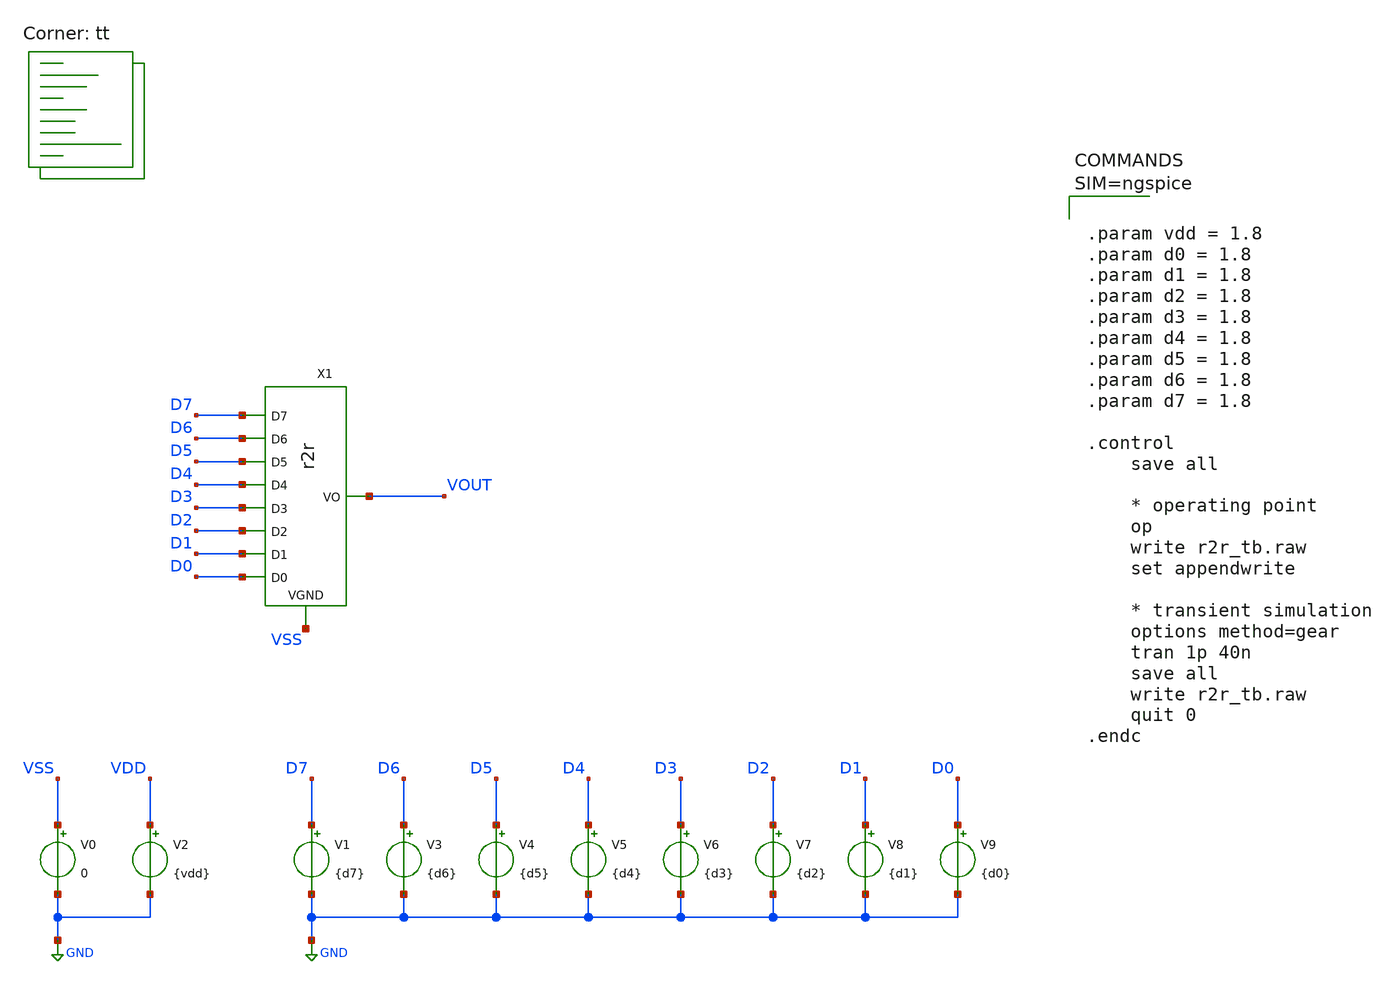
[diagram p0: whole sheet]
** sch_path: xschem/r2r_tb.sch
**.subckt r2r_tb
X1 D7 D6 D5 D4 D3 D2 D1 D0 VOUT VSS r2r
V0 VSS GND 0
V2 VDD GND {vdd}
V3 D6 GND {d6}
V1 D7 GND {d7}
V4 D5 GND {d5}
V5 D4 GND {d4}
V6 D3 GND {d3}
V7 D2 GND {d2}
V8 D1 GND {d1}
V9 D0 GND {d0}
**** begin user architecture code



.param vdd = 1.8
.param d0 = 1.8
.param d1 = 1.8
.param d2 = 1.8
.param d3 = 1.8
.param d4 = 1.8
.param d5 = 1.8
.param d6 = 1.8
.param d7 = 1.8

.control
    save all

    * operating point
    op
    write r2r_tb.raw
    set appendwrite

    * transient simulation
    options method=gear
    tran 1p 40n
    save all
    write r2r_tb.raw
    quit 0
.endc



.lib $::SKYWATER_MODELS/sky130.lib.spice tt
**** end user architecture code
**.ends

* expanding   symbol:  /home/unixpoly/analog/projects/sky130/r2r-dac/xschem/r2r.sym # of pins=10
** sym_path: xschem/r2r.sym
** sch_path: xschem/r2r.sch
.subckt r2r D7 D6 D5 D4 D3 D2 D1 D0 VO VGND
*.ipin D0
*.ipin D1
*.ipin D2
*.ipin D3
*.ipin D4
*.ipin D5
*.ipin D6
*.ipin D7
*.opin VO
*.iopin VGND
XR8 net1 VGND VGND sky130_fd_pr__res_high_po_1p41 L=50 mult=1 m=1
XR1 net2 net1 VGND sky130_fd_pr__res_high_po_1p41 L=50 mult=1 m=1
XR2 net3 D0 VGND sky130_fd_pr__res_high_po_1p41 L=50 mult=1 m=1
XR3 net2 net3 VGND sky130_fd_pr__res_high_po_1p41 L=50 mult=1 m=1
XR4 net2 net5 VGND sky130_fd_pr__res_high_po_1p41 L=50 mult=1 m=1
XR5 net4 D1 VGND sky130_fd_pr__res_high_po_1p41 L=50 mult=1 m=1
XR6 net5 net4 VGND sky130_fd_pr__res_high_po_1p41 L=50 mult=1 m=1
XR7 net5 net6 VGND sky130_fd_pr__res_high_po_1p41 L=50 mult=1 m=1
XR9 net7 D2 VGND sky130_fd_pr__res_high_po_1p41 L=50 mult=1 m=1
XR10 net6 net7 VGND sky130_fd_pr__res_high_po_1p41 L=50 mult=1 m=1
XR11 net6 net8 VGND sky130_fd_pr__res_high_po_1p41 L=50 mult=1 m=1
XR12 net9 D3 VGND sky130_fd_pr__res_high_po_1p41 L=50 mult=1 m=1
XR13 net8 net9 VGND sky130_fd_pr__res_high_po_1p41 L=50 mult=1 m=1
XR14 net8 net10 VGND sky130_fd_pr__res_high_po_1p41 L=50 mult=1 m=1
XR15 net11 D4 VGND sky130_fd_pr__res_high_po_1p41 L=50 mult=1 m=1
XR16 net10 net11 VGND sky130_fd_pr__res_high_po_1p41 L=50 mult=1 m=1
XR17 net10 net12 VGND sky130_fd_pr__res_high_po_1p41 L=50 mult=1 m=1
XR18 net13 D5 VGND sky130_fd_pr__res_high_po_1p41 L=50 mult=1 m=1
XR19 net12 net13 VGND sky130_fd_pr__res_high_po_1p41 L=50 mult=1 m=1
XR20 net12 net14 VGND sky130_fd_pr__res_high_po_1p41 L=50 mult=1 m=1
XR21 net15 D6 VGND sky130_fd_pr__res_high_po_1p41 L=50 mult=1 m=1
XR22 net14 net15 VGND sky130_fd_pr__res_high_po_1p41 L=50 mult=1 m=1
XR23 net14 VO VGND sky130_fd_pr__res_high_po_1p41 L=50 mult=1 m=1
XR24 net16 D7 VGND sky130_fd_pr__res_high_po_1p41 L=50 mult=1 m=1
XR25 VO net16 VGND sky130_fd_pr__res_high_po_1p41 L=50 mult=1 m=1
.ends

.GLOBAL GND
.end
